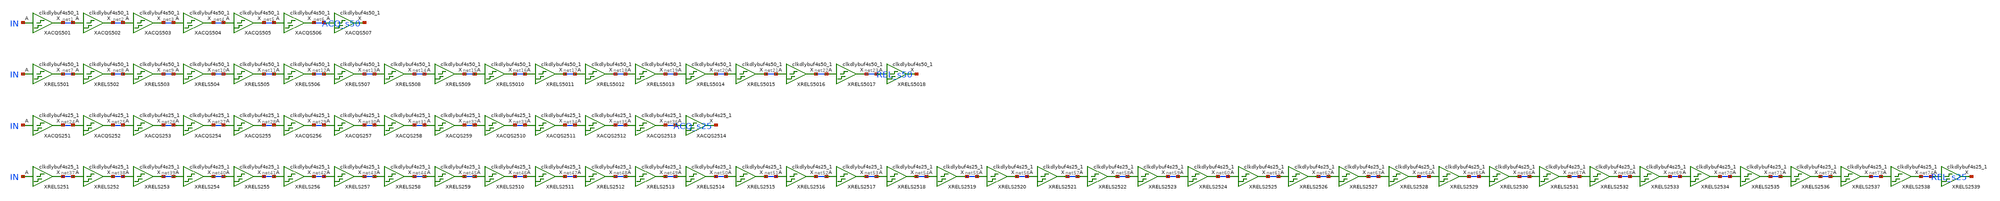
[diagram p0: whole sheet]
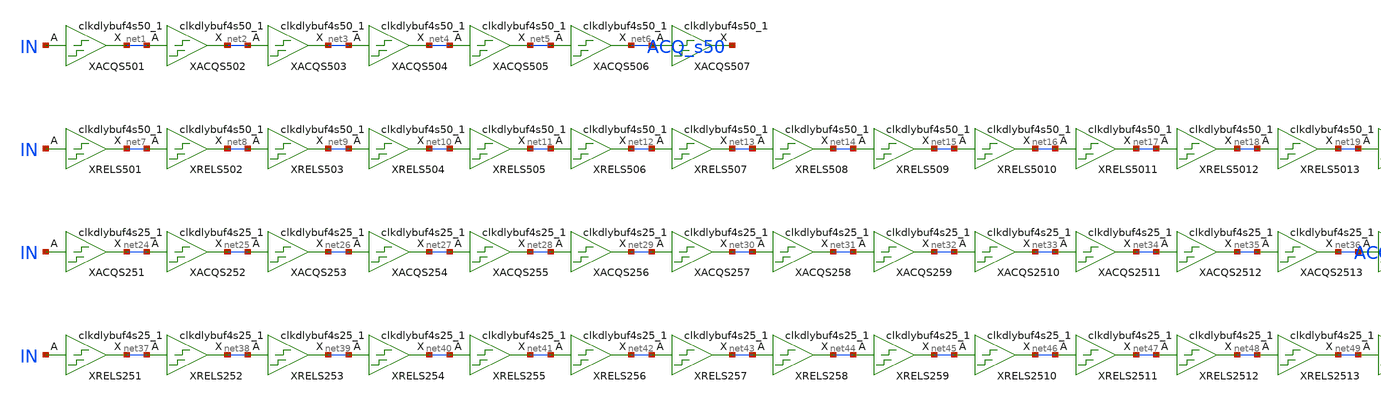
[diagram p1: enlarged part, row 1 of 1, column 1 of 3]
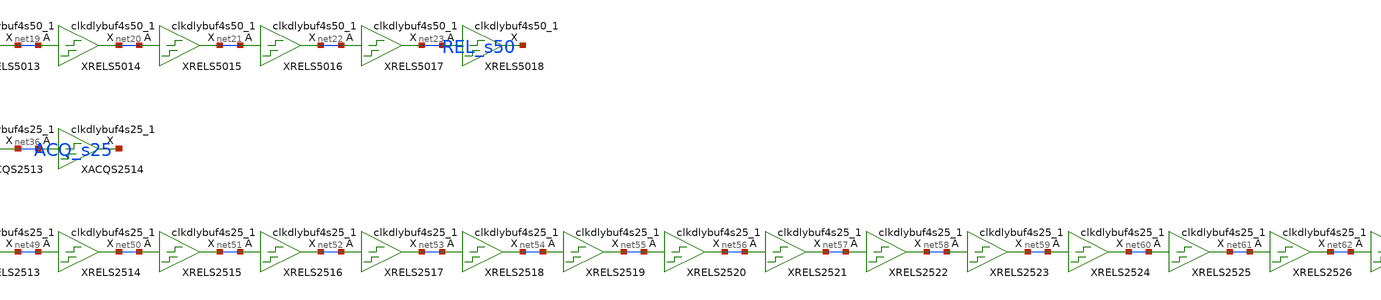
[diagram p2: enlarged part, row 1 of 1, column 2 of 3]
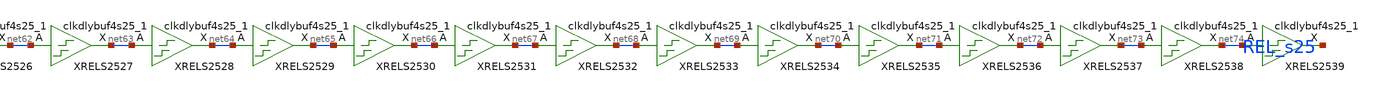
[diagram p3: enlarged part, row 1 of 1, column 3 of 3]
** sch_path: design/lock-detector/timing/phase_windows.sch
**.subckt phase_windows
XACQS501 IN GND GND VDD VDD net1 sky130_fd_sc_hd__clkdlybuf4s50_1
XACQS502 net1 GND GND VDD VDD net2 sky130_fd_sc_hd__clkdlybuf4s50_1
XACQS503 net2 GND GND VDD VDD net3 sky130_fd_sc_hd__clkdlybuf4s50_1
XACQS504 net3 GND GND VDD VDD net4 sky130_fd_sc_hd__clkdlybuf4s50_1
XACQS505 net4 GND GND VDD VDD net5 sky130_fd_sc_hd__clkdlybuf4s50_1
XACQS506 net5 GND GND VDD VDD net6 sky130_fd_sc_hd__clkdlybuf4s50_1
XACQS507 net6 GND GND VDD VDD ACQ_s50 sky130_fd_sc_hd__clkdlybuf4s50_1
XRELS501 IN GND GND VDD VDD net7 sky130_fd_sc_hd__clkdlybuf4s50_1
XRELS502 net7 GND GND VDD VDD net8 sky130_fd_sc_hd__clkdlybuf4s50_1
XRELS503 net8 GND GND VDD VDD net9 sky130_fd_sc_hd__clkdlybuf4s50_1
XRELS504 net9 GND GND VDD VDD net10 sky130_fd_sc_hd__clkdlybuf4s50_1
XRELS505 net10 GND GND VDD VDD net11 sky130_fd_sc_hd__clkdlybuf4s50_1
XRELS506 net11 GND GND VDD VDD net12 sky130_fd_sc_hd__clkdlybuf4s50_1
XRELS507 net12 GND GND VDD VDD net13 sky130_fd_sc_hd__clkdlybuf4s50_1
XRELS508 net13 GND GND VDD VDD net14 sky130_fd_sc_hd__clkdlybuf4s50_1
XRELS509 net14 GND GND VDD VDD net15 sky130_fd_sc_hd__clkdlybuf4s50_1
XRELS5010 net15 GND GND VDD VDD net16 sky130_fd_sc_hd__clkdlybuf4s50_1
XRELS5011 net16 GND GND VDD VDD net17 sky130_fd_sc_hd__clkdlybuf4s50_1
XRELS5012 net17 GND GND VDD VDD net18 sky130_fd_sc_hd__clkdlybuf4s50_1
XRELS5013 net18 GND GND VDD VDD net19 sky130_fd_sc_hd__clkdlybuf4s50_1
XRELS5014 net19 GND GND VDD VDD net20 sky130_fd_sc_hd__clkdlybuf4s50_1
XRELS5015 net20 GND GND VDD VDD net21 sky130_fd_sc_hd__clkdlybuf4s50_1
XRELS5016 net21 GND GND VDD VDD net22 sky130_fd_sc_hd__clkdlybuf4s50_1
XRELS5017 net22 GND GND VDD VDD net23 sky130_fd_sc_hd__clkdlybuf4s50_1
XRELS5018 net23 GND GND VDD VDD REL_s50 sky130_fd_sc_hd__clkdlybuf4s50_1
XACQS251 IN GND GND VDD VDD net24 sky130_fd_sc_hd__clkdlybuf4s25_1
XACQS252 net24 GND GND VDD VDD net25 sky130_fd_sc_hd__clkdlybuf4s25_1
XACQS253 net25 GND GND VDD VDD net26 sky130_fd_sc_hd__clkdlybuf4s25_1
XACQS254 net26 GND GND VDD VDD net27 sky130_fd_sc_hd__clkdlybuf4s25_1
XACQS255 net27 GND GND VDD VDD net28 sky130_fd_sc_hd__clkdlybuf4s25_1
XACQS256 net28 GND GND VDD VDD net29 sky130_fd_sc_hd__clkdlybuf4s25_1
XACQS257 net29 GND GND VDD VDD net30 sky130_fd_sc_hd__clkdlybuf4s25_1
XACQS258 net30 GND GND VDD VDD net31 sky130_fd_sc_hd__clkdlybuf4s25_1
XACQS259 net31 GND GND VDD VDD net32 sky130_fd_sc_hd__clkdlybuf4s25_1
XACQS2510 net32 GND GND VDD VDD net33 sky130_fd_sc_hd__clkdlybuf4s25_1
XACQS2511 net33 GND GND VDD VDD net34 sky130_fd_sc_hd__clkdlybuf4s25_1
XACQS2512 net34 GND GND VDD VDD net35 sky130_fd_sc_hd__clkdlybuf4s25_1
XACQS2513 net35 GND GND VDD VDD net36 sky130_fd_sc_hd__clkdlybuf4s25_1
XACQS2514 net36 GND GND VDD VDD ACQ_s25 sky130_fd_sc_hd__clkdlybuf4s25_1
XRELS251 IN GND GND VDD VDD net37 sky130_fd_sc_hd__clkdlybuf4s25_1
XRELS252 net37 GND GND VDD VDD net38 sky130_fd_sc_hd__clkdlybuf4s25_1
XRELS253 net38 GND GND VDD VDD net39 sky130_fd_sc_hd__clkdlybuf4s25_1
XRELS254 net39 GND GND VDD VDD net40 sky130_fd_sc_hd__clkdlybuf4s25_1
XRELS255 net40 GND GND VDD VDD net41 sky130_fd_sc_hd__clkdlybuf4s25_1
XRELS256 net41 GND GND VDD VDD net42 sky130_fd_sc_hd__clkdlybuf4s25_1
XRELS257 net42 GND GND VDD VDD net43 sky130_fd_sc_hd__clkdlybuf4s25_1
XRELS258 net43 GND GND VDD VDD net44 sky130_fd_sc_hd__clkdlybuf4s25_1
XRELS259 net44 GND GND VDD VDD net45 sky130_fd_sc_hd__clkdlybuf4s25_1
XRELS2510 net45 GND GND VDD VDD net46 sky130_fd_sc_hd__clkdlybuf4s25_1
XRELS2511 net46 GND GND VDD VDD net47 sky130_fd_sc_hd__clkdlybuf4s25_1
XRELS2512 net47 GND GND VDD VDD net48 sky130_fd_sc_hd__clkdlybuf4s25_1
XRELS2513 net48 GND GND VDD VDD net49 sky130_fd_sc_hd__clkdlybuf4s25_1
XRELS2514 net49 GND GND VDD VDD net50 sky130_fd_sc_hd__clkdlybuf4s25_1
XRELS2515 net50 GND GND VDD VDD net51 sky130_fd_sc_hd__clkdlybuf4s25_1
XRELS2516 net51 GND GND VDD VDD net52 sky130_fd_sc_hd__clkdlybuf4s25_1
XRELS2517 net52 GND GND VDD VDD net53 sky130_fd_sc_hd__clkdlybuf4s25_1
XRELS2518 net53 GND GND VDD VDD net54 sky130_fd_sc_hd__clkdlybuf4s25_1
XRELS2519 net54 GND GND VDD VDD net55 sky130_fd_sc_hd__clkdlybuf4s25_1
XRELS2520 net55 GND GND VDD VDD net56 sky130_fd_sc_hd__clkdlybuf4s25_1
XRELS2521 net56 GND GND VDD VDD net57 sky130_fd_sc_hd__clkdlybuf4s25_1
XRELS2522 net57 GND GND VDD VDD net58 sky130_fd_sc_hd__clkdlybuf4s25_1
XRELS2523 net58 GND GND VDD VDD net59 sky130_fd_sc_hd__clkdlybuf4s25_1
XRELS2524 net59 GND GND VDD VDD net60 sky130_fd_sc_hd__clkdlybuf4s25_1
XRELS2525 net60 GND GND VDD VDD net61 sky130_fd_sc_hd__clkdlybuf4s25_1
XRELS2526 net61 GND GND VDD VDD net62 sky130_fd_sc_hd__clkdlybuf4s25_1
XRELS2527 net62 GND GND VDD VDD net63 sky130_fd_sc_hd__clkdlybuf4s25_1
XRELS2528 net63 GND GND VDD VDD net64 sky130_fd_sc_hd__clkdlybuf4s25_1
XRELS2529 net64 GND GND VDD VDD net65 sky130_fd_sc_hd__clkdlybuf4s25_1
XRELS2530 net65 GND GND VDD VDD net66 sky130_fd_sc_hd__clkdlybuf4s25_1
XRELS2531 net66 GND GND VDD VDD net67 sky130_fd_sc_hd__clkdlybuf4s25_1
XRELS2532 net67 GND GND VDD VDD net68 sky130_fd_sc_hd__clkdlybuf4s25_1
XRELS2533 net68 GND GND VDD VDD net69 sky130_fd_sc_hd__clkdlybuf4s25_1
XRELS2534 net69 GND GND VDD VDD net70 sky130_fd_sc_hd__clkdlybuf4s25_1
XRELS2535 net70 GND GND VDD VDD net71 sky130_fd_sc_hd__clkdlybuf4s25_1
XRELS2536 net71 GND GND VDD VDD net72 sky130_fd_sc_hd__clkdlybuf4s25_1
XRELS2537 net72 GND GND VDD VDD net73 sky130_fd_sc_hd__clkdlybuf4s25_1
XRELS2538 net73 GND GND VDD VDD net74 sky130_fd_sc_hd__clkdlybuf4s25_1
XRELS2539 net74 GND GND VDD VDD REL_s25 sky130_fd_sc_hd__clkdlybuf4s25_1
**.ends
.end
